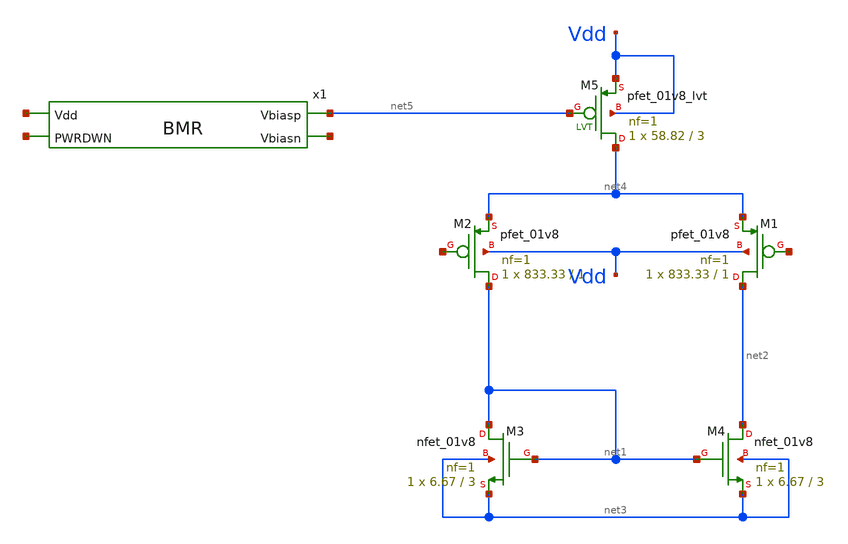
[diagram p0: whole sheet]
** sch_path: xschem/untitled-8.sch
**.subckt untitled-8
XM2 net1 net6 net4 Vdd sky130_fd_pr__pfet_01v8 L=1 W=833.33 nf=1 ad='int((1 + 1)/2) * 833.33 / 1 * 0.29'
+ as='int((1 + 2)/2) * 833.33 / 1 * 0.29' pd='2*int((1 + 1)/2) * (833.33 / 1 + 0.29)' ps='2*int((1 + 2)/2) * (833.33 / 1 + 0.29)'
+ nrd='0.29 / 833.33 ' nrs='0.29 / 833.33 ' sa=0 sb=0 sd=0 mult=1 m=1
XM1 net2 net7 net4 Vdd sky130_fd_pr__pfet_01v8 L=1 W=833.33 nf=1 ad='int((1 + 1)/2) * 833.33 / 1 * 0.29'
+ as='int((1 + 2)/2) * 833.33 / 1 * 0.29' pd='2*int((1 + 1)/2) * (833.33 / 1 + 0.29)' ps='2*int((1 + 2)/2) * (833.33 / 1 + 0.29)'
+ nrd='0.29 / 833.33 ' nrs='0.29 / 833.33 ' sa=0 sb=0 sd=0 mult=1 m=1
XM3 net1 net1 net3 net3 sky130_fd_pr__nfet_01v8 L=3 W=6.67 nf=1 ad='int((1 + 1)/2) * 6.67 / 1 * 0.29'
+ as='int((1 + 2)/2) * 6.67 / 1 * 0.29' pd='2*int((1 + 1)/2) * (6.67 / 1 + 0.29)' ps='2*int((1 + 2)/2) * (6.67 / 1 + 0.29)'
+ nrd='0.29 / 6.67 ' nrs='0.29 / 6.67 ' sa=0 sb=0 sd=0 mult=1 m=1
XM4 net2 net1 net3 net3 sky130_fd_pr__nfet_01v8 L=3 W=6.67 nf=1 ad='int((1 + 1)/2) * 6.67 / 1 * 0.29'
+ as='int((1 + 2)/2) * 6.67 / 1 * 0.29' pd='2*int((1 + 1)/2) * (6.67 / 1 + 0.29)' ps='2*int((1 + 2)/2) * (6.67 / 1 + 0.29)'
+ nrd='0.29 / 6.67 ' nrs='0.29 / 6.67 ' sa=0 sb=0 sd=0 mult=1 m=1
XM5 net4 net5 Vdd Vdd sky130_fd_pr__pfet_01v8_lvt L=3 W=58.82 nf=1 ad='int((1 + 1)/2) * 58.82 / 1 * 0.29'
+ as='int((1 + 2)/2) * 58.82 / 1 * 0.29' pd='2*int((1 + 1)/2) * (58.82 / 1 + 0.29)' ps='2*int((1 + 2)/2) * (58.82 / 1 + 0.29)'
+ nrd='0.29 / 58.82 ' nrs='0.29 / 58.82 ' sa=0 sb=0 sd=0 mult=1 m=1
x1 net8 net5 net9 net10 BMR
**.ends

* expanding   symbol:  BMR.sym # of pins=4
** sym_path: xschem/BMR.sym
** sch_path: xschem/BMR.sch
.subckt BMR Vdd Vbiasp Vbiasn PWRDWN
*.ipin Vdd
*.opin Vbiasn
*.opin Vbiasp
*.ipin PWRDWN
XM3 Vbiasn Vbiasn GND GND sky130_fd_pr__nfet_g5v0d10v5 L=3 W=1.4 nf=1 ad='int((1 + 1)/2) * 1.4 / 1 * 0.29'
+ as='int((1 + 2)/2) * 1.4 / 1 * 0.29' pd='2*int((1 + 1)/2) * (1.4 / 1 + 0.29)' ps='2*int((1 + 2)/2) * (1.4 / 1 + 0.29)'
+ nrd='0.29 / 1.4 ' nrs='0.29 / 1.4 ' sa=0 sb=0 sd=0 mult=1 m=1
XM1 Vbiasp Vbiasp Vdd Vdd sky130_fd_pr__pfet_g5v0d10v5 L=3 W=31 nf=8 ad='int((8 + 1)/2) * 31 / 8 * 0.29'
+ as='int((8 + 2)/2) * 31 / 8 * 0.29' pd='2*int((8 + 1)/2) * (31 / 8 + 0.29)' ps='2*int((8 + 2)/2) * (31 / 8 + 0.29)'
+ nrd='0.29 / 31 ' nrs='0.29 / 31 ' sa=0 sb=0 sd=0 mult=2 m=2
XM2 Vbiasn Vbiasp Vdd Vdd sky130_fd_pr__pfet_g5v0d10v5 L=3 W=31 nf=8 ad='int((8 + 1)/2) * 31 / 8 * 0.29'
+ as='int((8 + 2)/2) * 31 / 8 * 0.29' pd='2*int((8 + 1)/2) * (31 / 8 + 0.29)' ps='2*int((8 + 2)/2) * (31 / 8 + 0.29)'
+ nrd='0.29 / 31 ' nrs='0.29 / 31 ' sa=0 sb=0 sd=0 mult=2 m=2
XM11 net1 PWRUP Vdd Vdd sky130_fd_pr__pfet_g5v0d10v5 L=10 W=1 nf=1 ad='int((1 + 1)/2) * 1 / 1 * 0.29'
+ as='int((1 + 2)/2) * 1 / 1 * 0.29' pd='2*int((1 + 1)/2) * (1 / 1 + 0.29)' ps='2*int((1 + 2)/2) * (1 / 1 + 0.29)'
+ nrd='0.29 / 1 ' nrs='0.29 / 1 ' sa=0 sb=0 sd=0 mult=1 m=1
XM4 Vbiasp Vbiasn net2 GND sky130_fd_pr__nfet_g5v0d10v5 L=3 W=1.4 nf=1 ad='int((1 + 1)/2) * 1.4 / 1 * 0.29'
+ as='int((1 + 2)/2) * 1.4 / 1 * 0.29' pd='2*int((1 + 1)/2) * (1.4 / 1 + 0.29)' ps='2*int((1 + 2)/2) * (1.4 / 1 + 0.29)'
+ nrd='0.29 / 1.4 ' nrs='0.29 / 1.4 ' sa=0 sb=0 sd=0 mult=2 m=2
XM5 net1 Vbiasn GND GND sky130_fd_pr__nfet_g5v0d10v5 L=3 W=1.4 nf=1 ad='int((1 + 1)/2) * 1.4 / 1 * 0.29'
+ as='int((1 + 2)/2) * 1.4 / 1 * 0.29' pd='2*int((1 + 1)/2) * (1.4 / 1 + 0.29)' ps='2*int((1 + 2)/2) * (1.4 / 1 + 0.29)'
+ nrd='0.29 / 1.4 ' nrs='0.29 / 1.4 ' sa=0 sb=0 sd=0 mult=1 m=1
XM7 net3 net1 Vbiasn GND sky130_fd_pr__nfet_g5v0d10v5 L=1 W=20 nf=1 ad='int((1 + 1)/2) * 20 / 1 * 0.29'
+ as='int((1 + 2)/2) * 20 / 1 * 0.29' pd='2*int((1 + 1)/2) * (20 / 1 + 0.29)' ps='2*int((1 + 2)/2) * (20 / 1 + 0.29)'
+ nrd='0.29 / 20 ' nrs='0.29 / 20 ' sa=0 sb=0 sd=0 mult=1 m=1
x1 Vdd PWRUP PWRDWN GND NOT_GATE
XM12 Vbiasp PWRUP net3 GND sky130_fd_pr__nfet_g5v0d10v5 L=1 W=20 nf=1 ad='int((1 + 1)/2) * 20 / 1 * 0.29'
+ as='int((1 + 2)/2) * 20 / 1 * 0.29' pd='2*int((1 + 1)/2) * (20 / 1 + 0.29)' ps='2*int((1 + 2)/2) * (20 / 1 + 0.29)'
+ nrd='0.29 / 20 ' nrs='0.29 / 20 ' sa=0 sb=0 sd=0 mult=1 m=1
XM9 Vbiasp PWRUP Vdd Vdd sky130_fd_pr__pfet_g5v0d10v5 L=1 W=3 nf=1 ad='int((1 + 1)/2) * 3 / 1 * 0.29'
+ as='int((1 + 2)/2) * 3 / 1 * 0.29' pd='2*int((1 + 1)/2) * (3 / 1 + 0.29)' ps='2*int((1 + 2)/2) * (3 / 1 + 0.29)'
+ nrd='0.29 / 3 ' nrs='0.29 / 3 ' sa=0 sb=0 sd=0 mult=1 m=1
XM10 Vbiasn PWRDWN GND GND sky130_fd_pr__nfet_g5v0d10v5 L=1 W=1 nf=1 ad='int((1 + 1)/2) * 1 / 1 * 0.29'
+ as='int((1 + 2)/2) * 1 / 1 * 0.29' pd='2*int((1 + 1)/2) * (1 / 1 + 0.29)' ps='2*int((1 + 2)/2) * (1 / 1 + 0.29)'
+ nrd='0.29 / 1 ' nrs='0.29 / 1 ' sa=0 sb=0 sd=0 mult=1 m=1
XR5 GND net2 GND sky130_fd_pr__res_xhigh_po_2p85 L=71.25 mult=1 m=1
XC10 Vdd net1 sky130_fd_pr__cap_mim_m3_1 W=10 L=10 MF=5 m=5
XC2 Vdd Vbiasp sky130_fd_pr__cap_mim_m3_1 W=10 L=10 MF=5 m=5
XC1 Vbiasn GND sky130_fd_pr__cap_mim_m3_1 W=10 L=10 MF=5 m=5
.ends


* expanding   symbol:  NOT_GATE.sym # of pins=4
** sym_path: xschem/NOT_GATE.sym
** sch_path: xschem/NOT_GATE.sch
.subckt NOT_GATE Vdd Vout Vin Vss
*.opin Vout
*.ipin Vdd
*.ipin Vss
*.ipin Vin
XM1 Vout Vin Vss Vss sky130_fd_pr__nfet_g5v0d10v5 L=1 W=1 nf=1 ad='int((1 + 1)/2) * 1 / 1 * 0.29' as='int((1 + 2)/2) * 1 / 1 * 0.29'
+ pd='2*int((1 + 1)/2) * (1 / 1 + 0.29)' ps='2*int((1 + 2)/2) * (1 / 1 + 0.29)' nrd='0.29 / 1 ' nrs='0.29 / 1 '
+ sa=0 sb=0 sd=0 mult=1 m=1
XM2 Vout Vin Vdd Vdd sky130_fd_pr__pfet_g5v0d10v5 L=1 W=3 nf=1 ad='int((1 + 1)/2) * 3 / 1 * 0.29' as='int((1 + 2)/2) * 3 / 1 * 0.29'
+ pd='2*int((1 + 1)/2) * (3 / 1 + 0.29)' ps='2*int((1 + 2)/2) * (3 / 1 + 0.29)' nrd='0.29 / 3 ' nrs='0.29 / 3 '
+ sa=0 sb=0 sd=0 mult=1 m=1
.ends

.GLOBAL GND
.end
